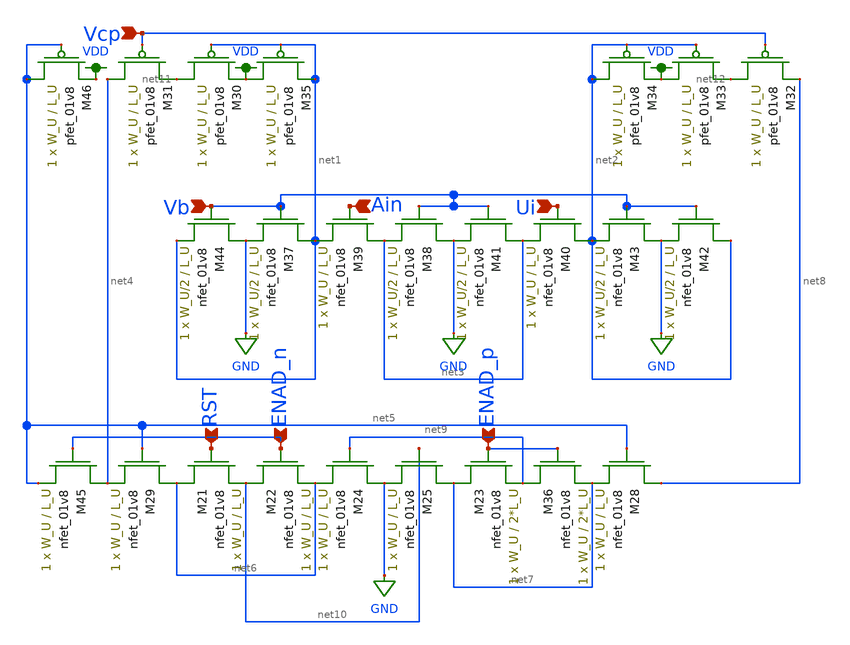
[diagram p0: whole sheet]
** sch_path: schematics/comp_lds.sch
**.subckt comp_lds RST ENAD_n ENAD_p Vcp Vb Ain Ui
*.ipin RST
*.ipin ENAD_n
*.ipin ENAD_p
*.ipin Vcp
*.ipin Vb
*.ipin Ain
*.ipin Ui
XM21 net6 RST net10 GND sky130_fd_pr__nfet_01v8 L=L_U W=W_U nf=1 ad='int((nf+1)/2) * W/nf * 0.29' as='int((nf+2)/2) * W/nf * 0.29'
+ pd='2*int((nf+1)/2) * (W/nf + 0.29)' ps='2*int((nf+2)/2) * (W/nf + 0.29)' nrd='0.29 / W' nrs='0.29 / W'
+ sa=0 sb=0 sd=0 mult=1 m=1
XM22 net10 ENAD_n net6 GND sky130_fd_pr__nfet_01v8 L=L_U W=W_U nf=1 ad='int((nf+1)/2) * W/nf * 0.29'
+ as='int((nf+2)/2) * W/nf * 0.29' pd='2*int((nf+1)/2) * (W/nf + 0.29)' ps='2*int((nf+2)/2) * (W/nf + 0.29)'
+ nrd='0.29 / W' nrs='0.29 / W' sa=0 sb=0 sd=0 mult=1 m=1
XM23 net7 ENAD_p net9 GND sky130_fd_pr__nfet_01v8 L=2*L_U W=W_U nf=1 ad='int((nf+1)/2) * W/nf * 0.29'
+ as='int((nf+2)/2) * W/nf * 0.29' pd='2*int((nf+1)/2) * (W/nf + 0.29)' ps='2*int((nf+2)/2) * (W/nf + 0.29)'
+ nrd='0.29 / W' nrs='0.29 / W' sa=0 sb=0 sd=0 mult=1 m=1
XM24 GND net9 net6 GND sky130_fd_pr__nfet_01v8 L=L_U W=W_U nf=1 ad='int((nf+1)/2) * W/nf * 0.29' as='int((nf+2)/2) * W/nf * 0.29'
+ pd='2*int((nf+1)/2) * (W/nf + 0.29)' ps='2*int((nf+2)/2) * (W/nf + 0.29)' nrd='0.29 / W' nrs='0.29 / W'
+ sa=0 sb=0 sd=0 mult=1 m=1
XM25 net7 net10 GND GND sky130_fd_pr__nfet_01v8 L=L_U W=W_U nf=1 ad='int((nf+1)/2) * W/nf * 0.29' as='int((nf+2)/2) * W/nf * 0.29'
+ pd='2*int((nf+1)/2) * (W/nf + 0.29)' ps='2*int((nf+2)/2) * (W/nf + 0.29)' nrd='0.29 / W' nrs='0.29 / W'
+ sa=0 sb=0 sd=0 mult=1 m=1
XM28 net8 net5 net7 GND sky130_fd_pr__nfet_01v8 L=L_U W=W_U nf=1 ad='int((nf+1)/2) * W/nf * 0.29' as='int((nf+2)/2) * W/nf * 0.29'
+ pd='2*int((nf+1)/2) * (W/nf + 0.29)' ps='2*int((nf+2)/2) * (W/nf + 0.29)' nrd='0.29 / W' nrs='0.29 / W'
+ sa=0 sb=0 sd=0 mult=1 m=1
XM29 net6 net5 net4 GND sky130_fd_pr__nfet_01v8 L=L_U W=W_U nf=1 ad='int((nf+1)/2) * W/nf * 0.29' as='int((nf+2)/2) * W/nf * 0.29'
+ pd='2*int((nf+1)/2) * (W/nf + 0.29)' ps='2*int((nf+2)/2) * (W/nf + 0.29)' nrd='0.29 / W' nrs='0.29 / W'
+ sa=0 sb=0 sd=0 mult=1 m=1
XM30 net11 net1 VDD VDD sky130_fd_pr__pfet_01v8 L=L_U W=W_U nf=1 ad='int((nf+1)/2) * W/nf * 0.29' as='int((nf+2)/2) * W/nf * 0.29'
+ pd='2*int((nf+1)/2) * (W/nf + 0.29)' ps='2*int((nf+2)/2) * (W/nf + 0.29)' nrd='0.29 / W' nrs='0.29 / W'
+ sa=0 sb=0 sd=0 mult=1 m=1
XM31 net4 Vcp net11 VDD sky130_fd_pr__pfet_01v8 L=L_U W=W_U nf=1 ad='int((nf+1)/2) * W/nf * 0.29' as='int((nf+2)/2) * W/nf * 0.29'
+ pd='2*int((nf+1)/2) * (W/nf + 0.29)' ps='2*int((nf+2)/2) * (W/nf + 0.29)' nrd='0.29 / W' nrs='0.29 / W'
+ sa=0 sb=0 sd=0 mult=1 m=1
XM32 net12 Vcp net8 VDD sky130_fd_pr__pfet_01v8 L=L_U W=W_U nf=1 ad='int((nf+1)/2) * W/nf * 0.29' as='int((nf+2)/2) * W/nf * 0.29'
+ pd='2*int((nf+1)/2) * (W/nf + 0.29)' ps='2*int((nf+2)/2) * (W/nf + 0.29)' nrd='0.29 / W' nrs='0.29 / W'
+ sa=0 sb=0 sd=0 mult=1 m=1
XM33 VDD net2 net12 VDD sky130_fd_pr__pfet_01v8 L=L_U W=W_U nf=1 ad='int((nf+1)/2) * W/nf * 0.29' as='int((nf+2)/2) * W/nf * 0.29'
+ pd='2*int((nf+1)/2) * (W/nf + 0.29)' ps='2*int((nf+2)/2) * (W/nf + 0.29)' nrd='0.29 / W' nrs='0.29 / W'
+ sa=0 sb=0 sd=0 mult=1 m=1
XM34 net2 net2 VDD VDD sky130_fd_pr__pfet_01v8 L=L_U W=W_U nf=1 ad='int((nf+1)/2) * W/nf * 0.29' as='int((nf+2)/2) * W/nf * 0.29'
+ pd='2*int((nf+1)/2) * (W/nf + 0.29)' ps='2*int((nf+2)/2) * (W/nf + 0.29)' nrd='0.29 / W' nrs='0.29 / W'
+ sa=0 sb=0 sd=0 mult=1 m=1
XM35 VDD net1 net1 VDD sky130_fd_pr__pfet_01v8 L=L_U W=W_U nf=1 ad='int((nf+1)/2) * W/nf * 0.29' as='int((nf+2)/2) * W/nf * 0.29'
+ pd='2*int((nf+1)/2) * (W/nf + 0.29)' ps='2*int((nf+2)/2) * (W/nf + 0.29)' nrd='0.29 / W' nrs='0.29 / W'
+ sa=0 sb=0 sd=0 mult=1 m=1
XM37 net1 Vb GND GND sky130_fd_pr__nfet_01v8 L=L_U W=W_U/2 nf=1 ad='int((nf+1)/2) * W/nf * 0.29' as='int((nf+2)/2) * W/nf * 0.29'
+ pd='2*int((nf+1)/2) * (W/nf + 0.29)' ps='2*int((nf+2)/2) * (W/nf + 0.29)' nrd='0.29 / W' nrs='0.29 / W'
+ sa=0 sb=0 sd=0 mult=1 m=1
XM38 GND Vb net3 GND sky130_fd_pr__nfet_01v8 L=L_U W=W_U/2 nf=1 ad='int((nf+1)/2) * W/nf * 0.29' as='int((nf+2)/2) * W/nf * 0.29'
+ pd='2*int((nf+1)/2) * (W/nf + 0.29)' ps='2*int((nf+2)/2) * (W/nf + 0.29)' nrd='0.29 / W' nrs='0.29 / W'
+ sa=0 sb=0 sd=0 mult=1 m=1
XM39 net3 Ain net1 GND sky130_fd_pr__nfet_01v8 L=L_U W=W_U nf=1 ad='int((nf+1)/2) * W/nf * 0.29' as='int((nf+2)/2) * W/nf * 0.29'
+ pd='2*int((nf+1)/2) * (W/nf + 0.29)' ps='2*int((nf+2)/2) * (W/nf + 0.29)' nrd='0.29 / W' nrs='0.29 / W'
+ sa=0 sb=0 sd=0 mult=1 m=1
XM40 net2 Ui net3 GND sky130_fd_pr__nfet_01v8 L=L_U W=W_U nf=1 ad='int((nf+1)/2) * W/nf * 0.29' as='int((nf+2)/2) * W/nf * 0.29'
+ pd='2*int((nf+1)/2) * (W/nf + 0.29)' ps='2*int((nf+2)/2) * (W/nf + 0.29)' nrd='0.29 / W' nrs='0.29 / W'
+ sa=0 sb=0 sd=0 mult=1 m=1
XM41 net3 Vb GND GND sky130_fd_pr__nfet_01v8 L=L_U W=W_U/2 nf=1 ad='int((nf+1)/2) * W/nf * 0.29' as='int((nf+2)/2) * W/nf * 0.29'
+ pd='2*int((nf+1)/2) * (W/nf + 0.29)' ps='2*int((nf+2)/2) * (W/nf + 0.29)' nrd='0.29 / W' nrs='0.29 / W'
+ sa=0 sb=0 sd=0 mult=1 m=1
XM42 net2 Vb GND GND sky130_fd_pr__nfet_01v8 L=L_U W=W_U/2 nf=1 ad='int((nf+1)/2) * W/nf * 0.29' as='int((nf+2)/2) * W/nf * 0.29'
+ pd='2*int((nf+1)/2) * (W/nf + 0.29)' ps='2*int((nf+2)/2) * (W/nf + 0.29)' nrd='0.29 / W' nrs='0.29 / W'
+ sa=0 sb=0 sd=0 mult=1 m=1
XM43 GND Vb net2 GND sky130_fd_pr__nfet_01v8 L=L_U W=W_U/2 nf=1 ad='int((nf+1)/2) * W/nf * 0.29' as='int((nf+2)/2) * W/nf * 0.29'
+ pd='2*int((nf+1)/2) * (W/nf + 0.29)' ps='2*int((nf+2)/2) * (W/nf + 0.29)' nrd='0.29 / W' nrs='0.29 / W'
+ sa=0 sb=0 sd=0 mult=1 m=1
XM44 GND Vb net1 GND sky130_fd_pr__nfet_01v8 L=L_U W=W_U/2 nf=1 ad='int((nf+1)/2) * W/nf * 0.29' as='int((nf+2)/2) * W/nf * 0.29'
+ pd='2*int((nf+1)/2) * (W/nf + 0.29)' ps='2*int((nf+2)/2) * (W/nf + 0.29)' nrd='0.29 / W' nrs='0.29 / W'
+ sa=0 sb=0 sd=0 mult=1 m=1
XM46 net5 net5 VDD VDD sky130_fd_pr__pfet_01v8 L=L_U W=W_U nf=1 ad='int((nf+1)/2) * W/nf * 0.29' as='int((nf+2)/2) * W/nf * 0.29'
+ pd='2*int((nf+1)/2) * (W/nf + 0.29)' ps='2*int((nf+2)/2) * (W/nf + 0.29)' nrd='0.29 / W' nrs='0.29 / W'
+ sa=0 sb=0 sd=0 mult=1 m=1
XM36 net9 ENAD_p net7 GND sky130_fd_pr__nfet_01v8 L=2*L_U W=W_U nf=1 ad='int((nf+1)/2) * W/nf * 0.29'
+ as='int((nf+2)/2) * W/nf * 0.29' pd='2*int((nf+1)/2) * (W/nf + 0.29)' ps='2*int((nf+2)/2) * (W/nf + 0.29)'
+ nrd='0.29 / W' nrs='0.29 / W' sa=0 sb=0 sd=0 mult=1 m=1
XM45 net4 ENAD_n net5 GND sky130_fd_pr__nfet_01v8 L=L_U W=W_U nf=1 ad='int((nf+1)/2) * W/nf * 0.29' as='int((nf+2)/2) * W/nf * 0.29'
+ pd='2*int((nf+1)/2) * (W/nf + 0.29)' ps='2*int((nf+2)/2) * (W/nf + 0.29)' nrd='0.29 / W' nrs='0.29 / W'
+ sa=0 sb=0 sd=0 mult=1 m=1
**.ends
.GLOBAL GND
.GLOBAL VDD
.end
